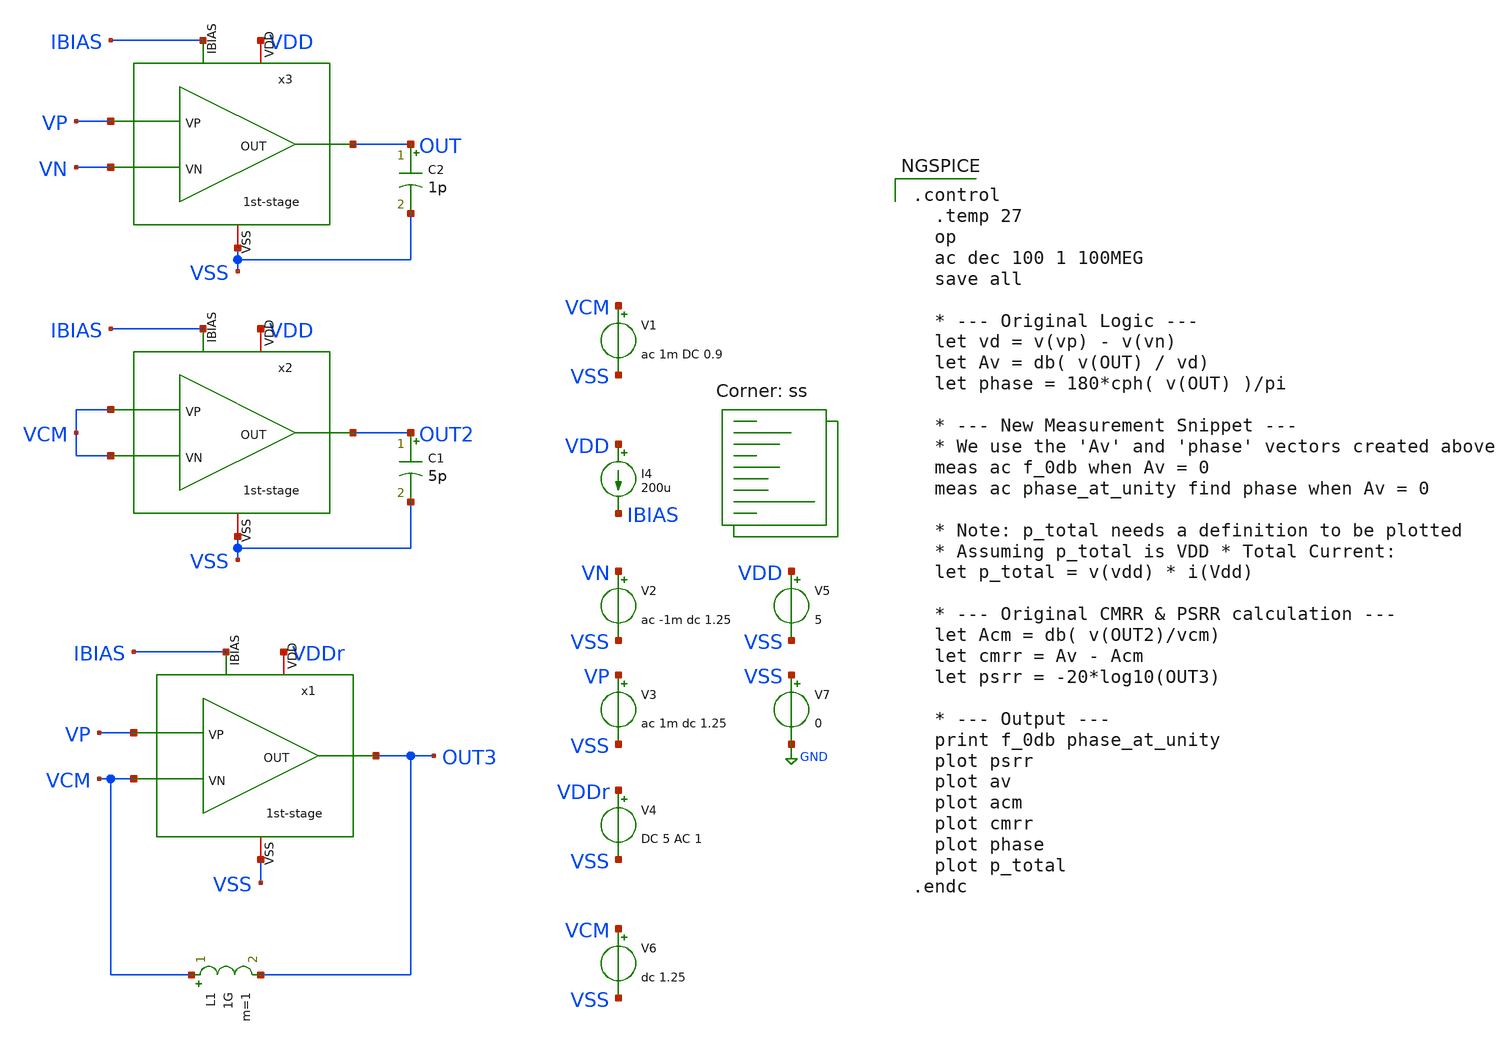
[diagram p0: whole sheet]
** sch_path: xschem/error-amplifier2/schematics/tb_ac.sch
**.subckt tb_ac
V2 VN VSS ac -1m dc 1.25
V3 VP VSS ac 1m dc 1.25
V5 VDD VSS 5
V7 VSS GND 0
C2 OUT VSS 1p m=1
I4 VDD IBIAS 200u
C1 OUT2 VSS 5p m=1
V1 VCM VSS ac 1m DC 0.9
V4 VDDr VSS DC 5 AC 1
x1 VDDr OUT3 VCM VP IBIAS VSS 1st-stage
x2 VDD OUT2 VCM VCM IBIAS VSS 1st-stage
x3 VDD OUT VN VP IBIAS VSS 1st-stage
L1 VCM OUT3 1G m=1
V6 VCM VSS dc 1.25
**** begin user architecture code

.control
  .temp 27
  op
  ac dec 100 1 100MEG
  save all

  * --- Original Logic ---
  let vd = v(vp) - v(vn)
  let Av = db( v(OUT) / vd)
  let phase = 180*cph( v(OUT) )/pi

  * --- New Measurement Snippet ---
  * We use the 'Av' and 'phase' vectors created above
  meas ac f_0db when Av = 0
  meas ac phase_at_unity find phase when Av = 0

  * Note: p_total needs a definition to be plotted
  * Assuming p_total is VDD * Total Current:
  let p_total = v(vdd) * i(Vdd)

  * --- Original CMRR & PSRR calculation ---
  let Acm = db( v(OUT2)/vcm)
  let cmrr = Av - Acm
  let psrr = -20*log10(OUT3)

  * --- Output ---
  print f_0db phase_at_unity
  plot psrr
  plot av
  plot acm
  plot cmrr
  plot phase
  plot p_total
.endc



.lib $::SKYWATER_MODELS/sky130.lib.spice ss
**** end user architecture code
**.ends

* expanding   symbol:  icdec-biomedical-pmic/xschem/error-amplifier2/schematics/1st-stage.sym # of
*+ pins=6
** sym_path: xschem/error-amplifier2/schematics/1st-stage.sym
** sch_path: xschem/error-amplifier2/schematics/1st-stage.sch
.subckt 1st-stage VDD OUT VN VP IBIAS VSS
*.iopin VDD
*.ipin VP
*.ipin VN
*.ipin IBIAS
*.iopin VSS
*.opin OUT
XM1 net2 net1 VDD VDD sky130_fd_pr__pfet_g5v0d10v5 L=1.25 W=75.2 nf=8 ad='int((nf+1)/2) * W/nf * 0.29'
+ as='int((nf+2)/2) * W/nf * 0.29' pd='2*int((nf+1)/2) * (W/nf + 0.29)' ps='2*int((nf+2)/2) * (W/nf + 0.29)'
+ nrd='0.29 / W' nrs='0.29 / W' sa=0 sb=0 sd=0 mult=1 m=1
XM2 net1 net1 VDD VDD sky130_fd_pr__pfet_g5v0d10v5 L=1.25 W=75.2 nf=8 ad='int((nf+1)/2) * W/nf * 0.29'
+ as='int((nf+2)/2) * W/nf * 0.29' pd='2*int((nf+1)/2) * (W/nf + 0.29)' ps='2*int((nf+2)/2) * (W/nf + 0.29)'
+ nrd='0.29 / W' nrs='0.29 / W' sa=0 sb=0 sd=0 mult=1 m=1
XM3 VDD VDD VDD VDD sky130_fd_pr__pfet_g5v0d10v5 L=0.5 W=18.8 nf=2 ad='int((nf+1)/2) * W/nf * 0.29' as='int((nf+2)/2) * W/nf * 0.29'
+ pd='2*int((nf+1)/2) * (W/nf + 0.29)' ps='2*int((nf+2)/2) * (W/nf + 0.29)' nrd='0.29 / W' nrs='0.29 / W'
+ sa=0 sb=0 sd=0 mult=1 m=1
XM4 VDD VDD VDD VDD sky130_fd_pr__pfet_g5v0d10v5 L=0.5 W=18.8 nf=2 ad='int((nf+1)/2) * W/nf * 0.29' as='int((nf+2)/2) * W/nf * 0.29'
+ pd='2*int((nf+1)/2) * (W/nf + 0.29)' ps='2*int((nf+2)/2) * (W/nf + 0.29)' nrd='0.29 / W' nrs='0.29 / W'
+ sa=0 sb=0 sd=0 mult=1 m=1
XM5 net2 VN net3 VSS sky130_fd_pr__nfet_g5v0d10v5 L=0.5 W=38 nf=2 ad='int((nf+1)/2) * W/nf * 0.29' as='int((nf+2)/2) * W/nf * 0.29'
+ pd='2*int((nf+1)/2) * (W/nf + 0.29)' ps='2*int((nf+2)/2) * (W/nf + 0.29)' nrd='0.29 / W' nrs='0.29 / W'
+ sa=0 sb=0 sd=0 mult=1 m=1
XM6 net1 VP net3 VSS sky130_fd_pr__nfet_g5v0d10v5 L=0.5 W=38 nf=2 ad='int((nf+1)/2) * W/nf * 0.29' as='int((nf+2)/2) * W/nf * 0.29'
+ pd='2*int((nf+1)/2) * (W/nf + 0.29)' ps='2*int((nf+2)/2) * (W/nf + 0.29)' nrd='0.29 / W' nrs='0.29 / W'
+ sa=0 sb=0 sd=0 mult=1 m=1
XM7 VSS VSS VSS VSS sky130_fd_pr__nfet_g5v0d10v5 L=0.5 W=9.5 nf=2 ad='int((nf+1)/2) * W/nf * 0.29' as='int((nf+2)/2) * W/nf * 0.29'
+ pd='2*int((nf+1)/2) * (W/nf + 0.29)' ps='2*int((nf+2)/2) * (W/nf + 0.29)' nrd='0.29 / W' nrs='0.29 / W'
+ sa=0 sb=0 sd=0 mult=1 m=1
XM8 VSS VSS VSS VSS sky130_fd_pr__nfet_g5v0d10v5 L=0.5 W=9.5 nf=2 ad='int((nf+1)/2) * W/nf * 0.29' as='int((nf+2)/2) * W/nf * 0.29'
+ pd='2*int((nf+1)/2) * (W/nf + 0.29)' ps='2*int((nf+2)/2) * (W/nf + 0.29)' nrd='0.29 / W' nrs='0.29 / W'
+ sa=0 sb=0 sd=0 mult=1 m=1
XM9 VSS VSS VSS VSS sky130_fd_pr__nfet_g5v0d10v5 L=0.5 W=9.5 nf=2 ad='int((nf+1)/2) * W/nf * 0.29' as='int((nf+2)/2) * W/nf * 0.29'
+ pd='2*int((nf+1)/2) * (W/nf + 0.29)' ps='2*int((nf+2)/2) * (W/nf + 0.29)' nrd='0.29 / W' nrs='0.29 / W'
+ sa=0 sb=0 sd=0 mult=1 m=1
XM10 VSS VSS VSS VSS sky130_fd_pr__nfet_g5v0d10v5 L=0.5 W=9.5 nf=2 ad='int((nf+1)/2) * W/nf * 0.29' as='int((nf+2)/2) * W/nf * 0.29'
+ pd='2*int((nf+1)/2) * (W/nf + 0.29)' ps='2*int((nf+2)/2) * (W/nf + 0.29)' nrd='0.29 / W' nrs='0.29 / W'
+ sa=0 sb=0 sd=0 mult=1 m=1
XM11 VSS VSS VSS VSS sky130_fd_pr__nfet_g5v0d10v5 L=0.5 W=9.5 nf=2 ad='int((nf+1)/2) * W/nf * 0.29' as='int((nf+2)/2) * W/nf * 0.29'
+ pd='2*int((nf+1)/2) * (W/nf + 0.29)' ps='2*int((nf+2)/2) * (W/nf + 0.29)' nrd='0.29 / W' nrs='0.29 / W'
+ sa=0 sb=0 sd=0 mult=1 m=1
XM12 VSS VSS VSS VSS sky130_fd_pr__nfet_g5v0d10v5 L=0.5 W=9.5 nf=2 ad='int((nf+1)/2) * W/nf * 0.29' as='int((nf+2)/2) * W/nf * 0.29'
+ pd='2*int((nf+1)/2) * (W/nf + 0.29)' ps='2*int((nf+2)/2) * (W/nf + 0.29)' nrd='0.29 / W' nrs='0.29 / W'
+ sa=0 sb=0 sd=0 mult=1 m=1
XM13 VSS VSS VSS VSS sky130_fd_pr__nfet_g5v0d10v5 L=0.5 W=9.5 nf=2 ad='int((nf+1)/2) * W/nf * 0.29' as='int((nf+2)/2) * W/nf * 0.29'
+ pd='2*int((nf+1)/2) * (W/nf + 0.29)' ps='2*int((nf+2)/2) * (W/nf + 0.29)' nrd='0.29 / W' nrs='0.29 / W'
+ sa=0 sb=0 sd=0 mult=1 m=1
XM14 VSS VSS VSS VSS sky130_fd_pr__nfet_g5v0d10v5 L=0.5 W=9.5 nf=2 ad='int((nf+1)/2) * W/nf * 0.29' as='int((nf+2)/2) * W/nf * 0.29'
+ pd='2*int((nf+1)/2) * (W/nf + 0.29)' ps='2*int((nf+2)/2) * (W/nf + 0.29)' nrd='0.29 / W' nrs='0.29 / W'
+ sa=0 sb=0 sd=0 mult=1 m=1
XM15 VSS VSS VSS VSS sky130_fd_pr__nfet_g5v0d10v5 L=0.5 W=9.5 nf=2 ad='int((nf+1)/2) * W/nf * 0.29' as='int((nf+2)/2) * W/nf * 0.29'
+ pd='2*int((nf+1)/2) * (W/nf + 0.29)' ps='2*int((nf+2)/2) * (W/nf + 0.29)' nrd='0.29 / W' nrs='0.29 / W'
+ sa=0 sb=0 sd=0 mult=1 m=1
XM16 VSS VSS VSS VSS sky130_fd_pr__nfet_g5v0d10v5 L=0.5 W=9.5 nf=2 ad='int((nf+1)/2) * W/nf * 0.29' as='int((nf+2)/2) * W/nf * 0.29'
+ pd='2*int((nf+1)/2) * (W/nf + 0.29)' ps='2*int((nf+2)/2) * (W/nf + 0.29)' nrd='0.29 / W' nrs='0.29 / W'
+ sa=0 sb=0 sd=0 mult=1 m=1
XM17 VSS VSS VSS VSS sky130_fd_pr__nfet_g5v0d10v5 L=0.5 W=9.5 nf=2 ad='int((nf+1)/2) * W/nf * 0.29' as='int((nf+2)/2) * W/nf * 0.29'
+ pd='2*int((nf+1)/2) * (W/nf + 0.29)' ps='2*int((nf+2)/2) * (W/nf + 0.29)' nrd='0.29 / W' nrs='0.29 / W'
+ sa=0 sb=0 sd=0 mult=1 m=1
XM18 VSS VSS VSS VSS sky130_fd_pr__nfet_g5v0d10v5 L=0.5 W=9.5 nf=2 ad='int((nf+1)/2) * W/nf * 0.29' as='int((nf+2)/2) * W/nf * 0.29'
+ pd='2*int((nf+1)/2) * (W/nf + 0.29)' ps='2*int((nf+2)/2) * (W/nf + 0.29)' nrd='0.29 / W' nrs='0.29 / W'
+ sa=0 sb=0 sd=0 mult=1 m=1
XM19 VSS VSS VSS VSS sky130_fd_pr__nfet_g5v0d10v5 L=0.5 W=9.5 nf=2 ad='int((nf+1)/2) * W/nf * 0.29' as='int((nf+2)/2) * W/nf * 0.29'
+ pd='2*int((nf+1)/2) * (W/nf + 0.29)' ps='2*int((nf+2)/2) * (W/nf + 0.29)' nrd='0.29 / W' nrs='0.29 / W'
+ sa=0 sb=0 sd=0 mult=1 m=1
XM20 VSS VSS VSS VSS sky130_fd_pr__nfet_g5v0d10v5 L=0.5 W=9.5 nf=2 ad='int((nf+1)/2) * W/nf * 0.29' as='int((nf+2)/2) * W/nf * 0.29'
+ pd='2*int((nf+1)/2) * (W/nf + 0.29)' ps='2*int((nf+2)/2) * (W/nf + 0.29)' nrd='0.29 / W' nrs='0.29 / W'
+ sa=0 sb=0 sd=0 mult=1 m=1
XM21 VSS VSS VSS VSS sky130_fd_pr__nfet_g5v0d10v5 L=0.5 W=9.5 nf=2 ad='int((nf+1)/2) * W/nf * 0.29' as='int((nf+2)/2) * W/nf * 0.29'
+ pd='2*int((nf+1)/2) * (W/nf + 0.29)' ps='2*int((nf+2)/2) * (W/nf + 0.29)' nrd='0.29 / W' nrs='0.29 / W'
+ sa=0 sb=0 sd=0 mult=1 m=1
XM22 VSS VSS VSS VSS sky130_fd_pr__nfet_g5v0d10v5 L=0.5 W=9.5 nf=2 ad='int((nf+1)/2) * W/nf * 0.29' as='int((nf+2)/2) * W/nf * 0.29'
+ pd='2*int((nf+1)/2) * (W/nf + 0.29)' ps='2*int((nf+2)/2) * (W/nf + 0.29)' nrd='0.29 / W' nrs='0.29 / W'
+ sa=0 sb=0 sd=0 mult=1 m=1
XM23 net3 IBIAS VSS VSS sky130_fd_pr__nfet_g5v0d10v5 L=1.25 W=60 nf=4 ad='int((nf+1)/2) * W/nf * 0.29'
+ as='int((nf+2)/2) * W/nf * 0.29' pd='2*int((nf+1)/2) * (W/nf + 0.29)' ps='2*int((nf+2)/2) * (W/nf + 0.29)'
+ nrd='0.29 / W' nrs='0.29 / W' sa=0 sb=0 sd=0 mult=1 m=1
XM24 IBIAS IBIAS VSS VSS sky130_fd_pr__nfet_g5v0d10v5 L=1.25 W=60 nf=4 ad='int((nf+1)/2) * W/nf * 0.29'
+ as='int((nf+2)/2) * W/nf * 0.29' pd='2*int((nf+1)/2) * (W/nf + 0.29)' ps='2*int((nf+2)/2) * (W/nf + 0.29)'
+ nrd='0.29 / W' nrs='0.29 / W' sa=0 sb=0 sd=0 mult=1 m=1
XM25 VSS VSS VSS VSS sky130_fd_pr__nfet_g5v0d10v5 L=0.5 W=15 nf=2 ad='int((nf+1)/2) * W/nf * 0.29' as='int((nf+2)/2) * W/nf * 0.29'
+ pd='2*int((nf+1)/2) * (W/nf + 0.29)' ps='2*int((nf+2)/2) * (W/nf + 0.29)' nrd='0.29 / W' nrs='0.29 / W'
+ sa=0 sb=0 sd=0 mult=1 m=1
XM26 VSS VSS VSS VSS sky130_fd_pr__nfet_g5v0d10v5 L=0.5 W=15 nf=2 ad='int((nf+1)/2) * W/nf * 0.29' as='int((nf+2)/2) * W/nf * 0.29'
+ pd='2*int((nf+1)/2) * (W/nf + 0.29)' ps='2*int((nf+2)/2) * (W/nf + 0.29)' nrd='0.29 / W' nrs='0.29 / W'
+ sa=0 sb=0 sd=0 mult=1 m=1
XM27 OUT net2 VDD VDD sky130_fd_pr__pfet_g5v0d10v5 L=1.25 W=160 nf=16 ad='int((nf+1)/2) * W/nf * 0.29'
+ as='int((nf+2)/2) * W/nf * 0.29' pd='2*int((nf+1)/2) * (W/nf + 0.29)' ps='2*int((nf+2)/2) * (W/nf + 0.29)'
+ nrd='0.29 / W' nrs='0.29 / W' sa=0 sb=0 sd=0 mult=1 m=1
XM28 OUT IBIAS VSS VSS sky130_fd_pr__nfet_g5v0d10v5 L=1.25 W=60 nf=8 ad='int((nf+1)/2) * W/nf * 0.29'
+ as='int((nf+2)/2) * W/nf * 0.29' pd='2*int((nf+1)/2) * (W/nf + 0.29)' ps='2*int((nf+2)/2) * (W/nf + 0.29)'
+ nrd='0.29 / W' nrs='0.29 / W' sa=0 sb=0 sd=0 mult=1 m=1
XC1 net4 net2 sky130_fd_pr__cap_mim_m3_1 W=25 L=25 MF=8 m=8
XM29 OUT VSS net4 VDD sky130_fd_pr__pfet_g5v0d10v5 L=0.9 W=20 nf=4 ad='int((nf+1)/2) * W/nf * 0.29' as='int((nf+2)/2) * W/nf * 0.29'
+ pd='2*int((nf+1)/2) * (W/nf + 0.29)' ps='2*int((nf+2)/2) * (W/nf + 0.29)' nrd='0.29 / W' nrs='0.29 / W'
+ sa=0 sb=0 sd=0 mult=1 m=1
.ends

.GLOBAL GND
.end
